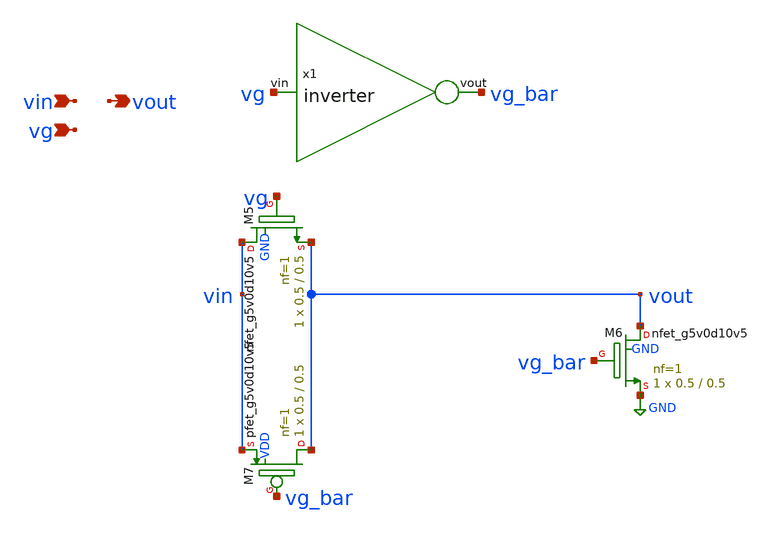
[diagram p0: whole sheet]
** sch_path: schematics/transmission_gate.sch
**.subckt transmission_gate vin vg vout
*.ipin vin
*.ipin vg
*.opin vout
x1 vg_bar vg inverter
XM5 vin vg vout GND sky130_fd_pr__nfet_g5v0d10v5 L=0.5 W=0.5 nf=1 ad='int((nf+1)/2) * W/nf * 0.29' as='int((nf+2)/2) * W/nf * 0.29'
+ pd='2*int((nf+1)/2) * (W/nf + 0.29)' ps='2*int((nf+2)/2) * (W/nf + 0.29)' nrd='0.29 / W' nrs='0.29 / W'
+ sa=0 sb=0 sd=0 mult=1 m=1
XM7 vout vg_bar vin VDD sky130_fd_pr__pfet_g5v0d10v5 L=0.5 W=0.5 nf=1 ad='int((nf+1)/2) * W/nf * 0.29'
+ as='int((nf+2)/2) * W/nf * 0.29' pd='2*int((nf+1)/2) * (W/nf + 0.29)' ps='2*int((nf+2)/2) * (W/nf + 0.29)'
+ nrd='0.29 / W' nrs='0.29 / W' sa=0 sb=0 sd=0 mult=1 m=1
XM6 vout vg_bar GND GND sky130_fd_pr__nfet_g5v0d10v5 L=0.5 W=0.5 nf=1 ad='int((nf+1)/2) * W/nf * 0.29'
+ as='int((nf+2)/2) * W/nf * 0.29' pd='2*int((nf+1)/2) * (W/nf + 0.29)' ps='2*int((nf+2)/2) * (W/nf + 0.29)'
+ nrd='0.29 / W' nrs='0.29 / W' sa=0 sb=0 sd=0 mult=1 m=1
**.ends

* expanding   symbol:  /media/sf_share/final_project/inverter.sym # of pins=2
** sym_path: schematics/inverter.sym
** sch_path: schematics/inverter.sch
.subckt inverter vout vin
*.ipin vin
*.opin vout
XM3 vout vin VDD VDD sky130_fd_pr__pfet_g5v0d10v5 L=0.5 W=0.5 nf=1 ad='int((nf+1)/2) * W/nf * 0.29' as='int((nf+2)/2) * W/nf * 0.29'
+ pd='2*int((nf+1)/2) * (W/nf + 0.29)' ps='2*int((nf+2)/2) * (W/nf + 0.29)' nrd='0.29 / W' nrs='0.29 / W'
+ sa=0 sb=0 sd=0 mult=1 m=1
XM5 vout vin GND GND sky130_fd_pr__nfet_g5v0d10v5 L=0.5 W=0.5 nf=1 ad='int((nf+1)/2) * W/nf * 0.29' as='int((nf+2)/2) * W/nf * 0.29'
+ pd='2*int((nf+1)/2) * (W/nf + 0.29)' ps='2*int((nf+2)/2) * (W/nf + 0.29)' nrd='0.29 / W' nrs='0.29 / W'
+ sa=0 sb=0 sd=0 mult=1 m=1
.ends

.GLOBAL GND
.GLOBAL VDD
.end
